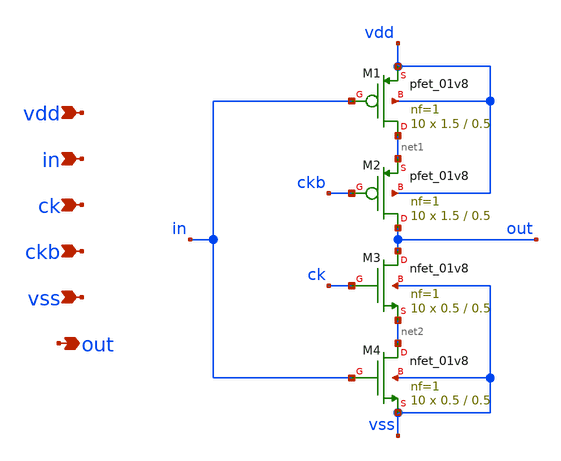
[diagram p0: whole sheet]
** sch_path: xschem/dac_sw_6.sch
**.subckt dac_sw_6 vdd in ck ckb vss out
*.ipin vdd
*.ipin in
*.ipin ck
*.ipin ckb
*.ipin vss
*.opin out
XM1 net1 in vdd vdd sky130_fd_pr__pfet_01v8 L=0.5 W=1.5 nf=1 ad='int((nf+1)/2) * W/nf * 0.29' as='int((nf+2)/2) * W/nf * 0.29'
+ pd='2*int((nf+1)/2) * (W/nf + 0.29)' ps='2*int((nf+2)/2) * (W/nf + 0.29)' nrd='0.29 / W' nrs='0.29 / W'
+ sa=0 sb=0 sd=0 mult=10 m=10
XM2 out ckb net1 vdd sky130_fd_pr__pfet_01v8 L=0.5 W=1.5 nf=1 ad='int((nf+1)/2) * W/nf * 0.29' as='int((nf+2)/2) * W/nf * 0.29'
+ pd='2*int((nf+1)/2) * (W/nf + 0.29)' ps='2*int((nf+2)/2) * (W/nf + 0.29)' nrd='0.29 / W' nrs='0.29 / W'
+ sa=0 sb=0 sd=0 mult=10 m=10
XM3 out ck net2 vss sky130_fd_pr__nfet_01v8 L=0.5 W=0.5 nf=1 ad='int((nf+1)/2) * W/nf * 0.29' as='int((nf+2)/2) * W/nf * 0.29'
+ pd='2*int((nf+1)/2) * (W/nf + 0.29)' ps='2*int((nf+2)/2) * (W/nf + 0.29)' nrd='0.29 / W' nrs='0.29 / W'
+ sa=0 sb=0 sd=0 mult=10 m=10
XM4 net2 in vss vss sky130_fd_pr__nfet_01v8 L=0.5 W=0.5 nf=1 ad='int((nf+1)/2) * W/nf * 0.29' as='int((nf+2)/2) * W/nf * 0.29'
+ pd='2*int((nf+1)/2) * (W/nf + 0.29)' ps='2*int((nf+2)/2) * (W/nf + 0.29)' nrd='0.29 / W' nrs='0.29 / W'
+ sa=0 sb=0 sd=0 mult=10 m=10
**.ends
.end
